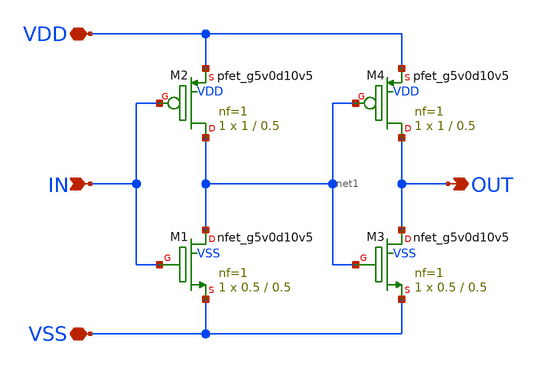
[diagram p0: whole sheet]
** sch_path: xschem/buffer.sch
**.subckt buffer VDD VSS IN OUT
*.iopin VDD
*.iopin VSS
*.ipin IN
*.opin OUT
XM1 net1 IN VSS VSS sky130_fd_pr__nfet_g5v0d10v5 L=0.5 W=0.5 nf=1 ad='int((nf+1)/2) * W/nf * 0.29' as='int((nf+2)/2) * W/nf * 0.29'
+ pd='2*int((nf+1)/2) * (W/nf + 0.29)' ps='2*int((nf+2)/2) * (W/nf + 0.29)' nrd='0.29 / W' nrs='0.29 / W'
+ sa=0 sb=0 sd=0 mult=1 m=1
XM2 net1 IN VDD VDD sky130_fd_pr__pfet_g5v0d10v5 L=0.5 W=1 nf=1 ad='int((nf+1)/2) * W/nf * 0.29' as='int((nf+2)/2) * W/nf * 0.29'
+ pd='2*int((nf+1)/2) * (W/nf + 0.29)' ps='2*int((nf+2)/2) * (W/nf + 0.29)' nrd='0.29 / W' nrs='0.29 / W'
+ sa=0 sb=0 sd=0 mult=1 m=1
XM3 OUT net1 VSS VSS sky130_fd_pr__nfet_g5v0d10v5 L=0.5 W=0.5 nf=1 ad='int((nf+1)/2) * W/nf * 0.29' as='int((nf+2)/2) * W/nf * 0.29'
+ pd='2*int((nf+1)/2) * (W/nf + 0.29)' ps='2*int((nf+2)/2) * (W/nf + 0.29)' nrd='0.29 / W' nrs='0.29 / W'
+ sa=0 sb=0 sd=0 mult=1 m=1
XM4 OUT net1 VDD VDD sky130_fd_pr__pfet_g5v0d10v5 L=0.5 W=1 nf=1 ad='int((nf+1)/2) * W/nf * 0.29' as='int((nf+2)/2) * W/nf * 0.29'
+ pd='2*int((nf+1)/2) * (W/nf + 0.29)' ps='2*int((nf+2)/2) * (W/nf + 0.29)' nrd='0.29 / W' nrs='0.29 / W'
+ sa=0 sb=0 sd=0 mult=1 m=1
**.ends
.end
